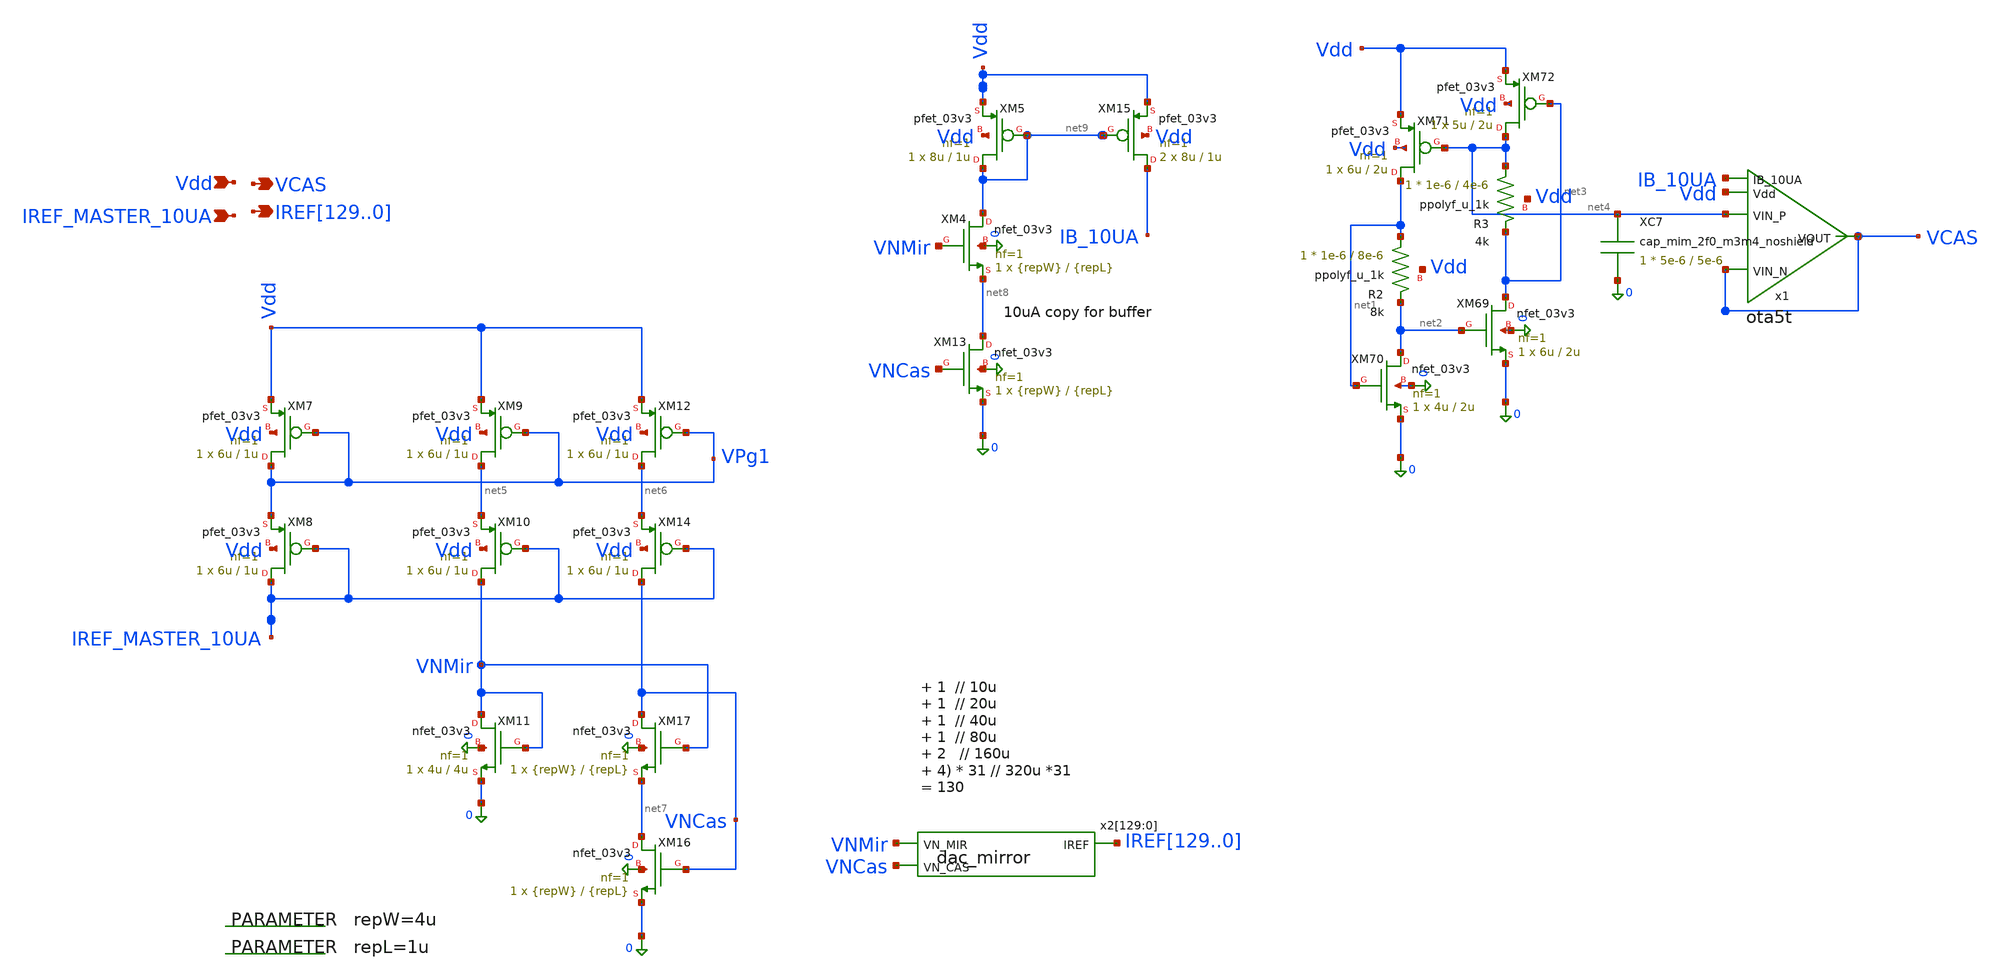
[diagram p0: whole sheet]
** sch_path: blocks/dac/iref/dac_iref.sch
**.subckt dac_iref Vdd VCAS
*+ IREF129,IREF128,IREF127,IREF126,IREF125,IREF124,IREF123,IREF122,IREF121,IREF120,IREF119,IREF118,IREF117,IREF116,IREF115,IREF114,IREF113,IREF112,IREF111,IREF110,IREF109,IREF108,IREF107,IREF106,IREF105,IREF104,IREF103,IREF102,IREF101,IREF100,IREF99,IREF98,IREF97,IREF96,IREF95,IREF94,IREF93,IREF92,IREF91,IREF90,IREF89,IREF88,IREF87,IREF86,IREF85,IREF84,IREF83,IREF82,IREF81,IREF80,IREF79,IREF78,IREF77,IREF76,IREF75,IREF74,IREF73,IREF72,IREF71,IREF70,IREF69,IREF68,IREF67,IREF66,IREF65,IREF64,IREF63,IREF62,IREF61,IREF60,IREF59,IREF58,IREF57,IREF56,IREF55,IREF54,IREF53,IREF52,IREF51,IREF50,IREF49,IREF48,IREF47,IREF46,IREF45,IREF44,IREF43,IREF42,IREF41,IREF40,IREF39,IREF38,IREF37,IREF36,IREF35,IREF34,IREF33,IREF32,IREF31,IREF30,IREF29,IREF28,IREF27,IREF26,IREF25,IREF24,IREF23,IREF22,IREF21,IREF20,IREF19,IREF18,IREF17,IREF16,IREF15,IREF14,IREF13,IREF12,IREF11,IREF10,IREF9,IREF8,IREF7,IREF6,IREF5,IREF4,IREF3,IREF2,IREF1,IREF0 IREF_MASTER_10UA
*.ipin Vdd
*.opin VCAS
*.opin
*+ IREF129,IREF128,IREF127,IREF126,IREF125,IREF124,IREF123,IREF122,IREF121,IREF120,IREF119,IREF118,IREF117,IREF116,IREF115,IREF114,IREF113,IREF112,IREF111,IREF110,IREF109,IREF108,IREF107,IREF106,IREF105,IREF104,IREF103,IREF102,IREF101,IREF100,IREF99,IREF98,IREF97,IREF96,IREF95,IREF94,IREF93,IREF92,IREF91,IREF90,IREF89,IREF88,IREF87,IREF86,IREF85,IREF84,IREF83,IREF82,IREF81,IREF80,IREF79,IREF78,IREF77,IREF76,IREF75,IREF74,IREF73,IREF72,IREF71,IREF70,IREF69,IREF68,IREF67,IREF66,IREF65,IREF64,IREF63,IREF62,IREF61,IREF60,IREF59,IREF58,IREF57,IREF56,IREF55,IREF54,IREF53,IREF52,IREF51,IREF50,IREF49,IREF48,IREF47,IREF46,IREF45,IREF44,IREF43,IREF42,IREF41,IREF40,IREF39,IREF38,IREF37,IREF36,IREF35,IREF34,IREF33,IREF32,IREF31,IREF30,IREF29,IREF28,IREF27,IREF26,IREF25,IREF24,IREF23,IREF22,IREF21,IREF20,IREF19,IREF18,IREF17,IREF16,IREF15,IREF14,IREF13,IREF12,IREF11,IREF10,IREF9,IREF8,IREF7,IREF6,IREF5,IREF4,IREF3,IREF2,IREF1,IREF0
*.ipin IREF_MASTER_10UA
XM69 net3 net2 0 0 nfet_03v3 L=2u W=6u nf=1 ad='int((nf+1)/2) * W/nf * 0.18u' as='int((nf+2)/2) * W/nf * 0.18u'
+ pd='2*int((nf+1)/2) * (W/nf + 0.18u)' ps='2*int((nf+2)/2) * (W/nf + 0.18u)' nrd='0.18u / W' nrs='0.18u / W'
+ sa=0 sb=0 sd=0 m=1
XM70 net2 net1 0 0 nfet_03v3 L=2u W=4u nf=1 ad='int((nf+1)/2) * W/nf * 0.18u' as='int((nf+2)/2) * W/nf * 0.18u'
+ pd='2*int((nf+1)/2) * (W/nf + 0.18u)' ps='2*int((nf+2)/2) * (W/nf + 0.18u)' nrd='0.18u / W' nrs='0.18u / W'
+ sa=0 sb=0 sd=0 m=1
XM71 net1 net4 Vdd Vdd pfet_03v3 L=2u W=6u nf=1 ad='int((nf+1)/2) * W/nf * 0.18u' as='int((nf+2)/2) * W/nf * 0.18u'
+ pd='2*int((nf+1)/2) * (W/nf + 0.18u)' ps='2*int((nf+2)/2) * (W/nf + 0.18u)' nrd='0.18u / W' nrs='0.18u / W'
+ sa=0 sb=0 sd=0 m=1
XM72 net4 net3 Vdd Vdd pfet_03v3 L=2u W=5u nf=1 ad='int((nf+1)/2) * W/nf * 0.18u' as='int((nf+2)/2) * W/nf * 0.18u'
+ pd='2*int((nf+1)/2) * (W/nf + 0.18u)' ps='2*int((nf+2)/2) * (W/nf + 0.18u)' nrd='0.18u / W' nrs='0.18u / W'
+ sa=0 sb=0 sd=0 m=1
x1 Vdd VCAS net4 VCAS IB_10UA ota5t
XC7 net4 0 cap_mim_2f0_m3m4_noshield c_width=5e-6 c_length=5e-6 m=1
XM7 VPg1 VPg1 Vdd Vdd pfet_03v3 L=1u W=6u nf=1 ad='int((nf+1)/2) * W/nf * 0.18u' as='int((nf+2)/2) * W/nf * 0.18u'
+ pd='2*int((nf+1)/2) * (W/nf + 0.18u)' ps='2*int((nf+2)/2) * (W/nf + 0.18u)' nrd='0.18u / W' nrs='0.18u / W'
+ sa=0 sb=0 sd=0 m=1
XM8 IREF_MASTER_10UA IREF_MASTER_10UA VPg1 Vdd pfet_03v3 L=1u W=6u nf=1 ad='int((nf+1)/2) * W/nf * 0.18u'
+ as='int((nf+2)/2) * W/nf * 0.18u' pd='2*int((nf+1)/2) * (W/nf + 0.18u)' ps='2*int((nf+2)/2) * (W/nf + 0.18u)'
+ nrd='0.18u / W' nrs='0.18u / W' sa=0 sb=0 sd=0 m=1
XM9 net5 VPg1 Vdd Vdd pfet_03v3 L=1u W=6u nf=1 ad='int((nf+1)/2) * W/nf * 0.18u' as='int((nf+2)/2) * W/nf * 0.18u'
+ pd='2*int((nf+1)/2) * (W/nf + 0.18u)' ps='2*int((nf+2)/2) * (W/nf + 0.18u)' nrd='0.18u / W' nrs='0.18u / W'
+ sa=0 sb=0 sd=0 m=1
XM10 VNMir IREF_MASTER_10UA net5 Vdd pfet_03v3 L=1u W=6u nf=1 ad='int((nf+1)/2) * W/nf * 0.18u' as='int((nf+2)/2) * W/nf * 0.18u'
+ pd='2*int((nf+1)/2) * (W/nf + 0.18u)' ps='2*int((nf+2)/2) * (W/nf + 0.18u)' nrd='0.18u / W' nrs='0.18u / W'
+ sa=0 sb=0 sd=0 m=1
XM11 VNMir VNMir 0 0 nfet_03v3 L=4u W=4u nf=1 ad='int((nf+1)/2) * W/nf * 0.18u' as='int((nf+2)/2) * W/nf * 0.18u'
+ pd='2*int((nf+1)/2) * (W/nf + 0.18u)' ps='2*int((nf+2)/2) * (W/nf + 0.18u)' nrd='0.18u / W' nrs='0.18u / W'
+ sa=0 sb=0 sd=0 m=1
XM12 net6 VPg1 Vdd Vdd pfet_03v3 L=1u W=6u nf=1 ad='int((nf+1)/2) * W/nf * 0.18u' as='int((nf+2)/2) * W/nf * 0.18u'
+ pd='2*int((nf+1)/2) * (W/nf + 0.18u)' ps='2*int((nf+2)/2) * (W/nf + 0.18u)' nrd='0.18u / W' nrs='0.18u / W'
+ sa=0 sb=0 sd=0 m=1
XM14 VNCas IREF_MASTER_10UA net6 Vdd pfet_03v3 L=1u W=6u nf=1 ad='int((nf+1)/2) * W/nf * 0.18u' as='int((nf+2)/2) * W/nf * 0.18u'
+ pd='2*int((nf+1)/2) * (W/nf + 0.18u)' ps='2*int((nf+2)/2) * (W/nf + 0.18u)' nrd='0.18u / W' nrs='0.18u / W'
+ sa=0 sb=0 sd=0 m=1
XM16 net7 VNCas 0 0 nfet_03v3 L={repL} W={repW} nf=1 ad='int((nf+1)/2) * W/nf * 0.18u' as='int((nf+2)/2) * W/nf * 0.18u'
+ pd='2*int((nf+1)/2) * (W/nf + 0.18u)' ps='2*int((nf+2)/2) * (W/nf + 0.18u)' nrd='0.18u / W' nrs='0.18u / W'
+ sa=0 sb=0 sd=0 m=1
XM17 VNCas VNMir net7 0 nfet_03v3 L={repL} W={repW} nf=1 ad='int((nf+1)/2) * W/nf * 0.18u' as='int((nf+2)/2) * W/nf * 0.18u'
+ pd='2*int((nf+1)/2) * (W/nf + 0.18u)' ps='2*int((nf+2)/2) * (W/nf + 0.18u)' nrd='0.18u / W' nrs='0.18u / W'
+ sa=0 sb=0 sd=0 m=1
XM4 net9 VNMir net8 0 nfet_03v3 L={repL} W={repW} nf=1 ad='int((nf+1)/2) * W/nf * 0.18u' as='int((nf+2)/2) * W/nf * 0.18u'
+ pd='2*int((nf+1)/2) * (W/nf + 0.18u)' ps='2*int((nf+2)/2) * (W/nf + 0.18u)' nrd='0.18u / W' nrs='0.18u / W'
+ sa=0 sb=0 sd=0 m=1
XM5 net9 net9 Vdd Vdd pfet_03v3 L=1u W=8u nf=1 ad='int((nf+1)/2) * W/nf * 0.18u' as='int((nf+2)/2) * W/nf * 0.18u'
+ pd='2*int((nf+1)/2) * (W/nf + 0.18u)' ps='2*int((nf+2)/2) * (W/nf + 0.18u)' nrd='0.18u / W' nrs='0.18u / W'
+ sa=0 sb=0 sd=0 m=1
XM13 net8 VNCas 0 0 nfet_03v3 L={repL} W={repW} nf=1 ad='int((nf+1)/2) * W/nf * 0.18u' as='int((nf+2)/2) * W/nf * 0.18u'
+ pd='2*int((nf+1)/2) * (W/nf + 0.18u)' ps='2*int((nf+2)/2) * (W/nf + 0.18u)' nrd='0.18u / W' nrs='0.18u / W'
+ sa=0 sb=0 sd=0 m=1
XR3 net4 net3 Vdd ppolyf_u_1k r_width=1e-6 r_length=4e-6 m=1
XR2 net1 net2 Vdd ppolyf_u_1k r_width=1e-6 r_length=8e-6 m=1
.param repW=4u
.param repL=1u
XM15 IB_10UA net9 Vdd Vdd pfet_03v3 L=1u W=8u nf=1 ad='int((nf+1)/2) * W/nf * 0.18u' as='int((nf+2)/2) * W/nf * 0.18u'
+ pd='2*int((nf+1)/2) * (W/nf + 0.18u)' ps='2*int((nf+2)/2) * (W/nf + 0.18u)' nrd='0.18u / W' nrs='0.18u / W'
+ sa=0 sb=0 sd=0 m=2
x2[129] VNMir IREF129 VNCas dac_mirror
x2[128] VNMir IREF128 VNCas dac_mirror
x2[127] VNMir IREF127 VNCas dac_mirror
x2[126] VNMir IREF126 VNCas dac_mirror
x2[125] VNMir IREF125 VNCas dac_mirror
x2[124] VNMir IREF124 VNCas dac_mirror
x2[123] VNMir IREF123 VNCas dac_mirror
x2[122] VNMir IREF122 VNCas dac_mirror
x2[121] VNMir IREF121 VNCas dac_mirror
x2[120] VNMir IREF120 VNCas dac_mirror
x2[119] VNMir IREF119 VNCas dac_mirror
x2[118] VNMir IREF118 VNCas dac_mirror
x2[117] VNMir IREF117 VNCas dac_mirror
x2[116] VNMir IREF116 VNCas dac_mirror
x2[115] VNMir IREF115 VNCas dac_mirror
x2[114] VNMir IREF114 VNCas dac_mirror
x2[113] VNMir IREF113 VNCas dac_mirror
x2[112] VNMir IREF112 VNCas dac_mirror
x2[111] VNMir IREF111 VNCas dac_mirror
x2[110] VNMir IREF110 VNCas dac_mirror
x2[109] VNMir IREF109 VNCas dac_mirror
x2[108] VNMir IREF108 VNCas dac_mirror
x2[107] VNMir IREF107 VNCas dac_mirror
x2[106] VNMir IREF106 VNCas dac_mirror
x2[105] VNMir IREF105 VNCas dac_mirror
x2[104] VNMir IREF104 VNCas dac_mirror
x2[103] VNMir IREF103 VNCas dac_mirror
x2[102] VNMir IREF102 VNCas dac_mirror
x2[101] VNMir IREF101 VNCas dac_mirror
x2[100] VNMir IREF100 VNCas dac_mirror
x2[99] VNMir IREF99 VNCas dac_mirror
x2[98] VNMir IREF98 VNCas dac_mirror
x2[97] VNMir IREF97 VNCas dac_mirror
x2[96] VNMir IREF96 VNCas dac_mirror
x2[95] VNMir IREF95 VNCas dac_mirror
x2[94] VNMir IREF94 VNCas dac_mirror
x2[93] VNMir IREF93 VNCas dac_mirror
x2[92] VNMir IREF92 VNCas dac_mirror
x2[91] VNMir IREF91 VNCas dac_mirror
x2[90] VNMir IREF90 VNCas dac_mirror
x2[89] VNMir IREF89 VNCas dac_mirror
x2[88] VNMir IREF88 VNCas dac_mirror
x2[87] VNMir IREF87 VNCas dac_mirror
x2[86] VNMir IREF86 VNCas dac_mirror
x2[85] VNMir IREF85 VNCas dac_mirror
x2[84] VNMir IREF84 VNCas dac_mirror
x2[83] VNMir IREF83 VNCas dac_mirror
x2[82] VNMir IREF82 VNCas dac_mirror
x2[81] VNMir IREF81 VNCas dac_mirror
x2[80] VNMir IREF80 VNCas dac_mirror
x2[79] VNMir IREF79 VNCas dac_mirror
x2[78] VNMir IREF78 VNCas dac_mirror
x2[77] VNMir IREF77 VNCas dac_mirror
x2[76] VNMir IREF76 VNCas dac_mirror
x2[75] VNMir IREF75 VNCas dac_mirror
x2[74] VNMir IREF74 VNCas dac_mirror
x2[73] VNMir IREF73 VNCas dac_mirror
x2[72] VNMir IREF72 VNCas dac_mirror
x2[71] VNMir IREF71 VNCas dac_mirror
x2[70] VNMir IREF70 VNCas dac_mirror
x2[69] VNMir IREF69 VNCas dac_mirror
x2[68] VNMir IREF68 VNCas dac_mirror
x2[67] VNMir IREF67 VNCas dac_mirror
x2[66] VNMir IREF66 VNCas dac_mirror
x2[65] VNMir IREF65 VNCas dac_mirror
x2[64] VNMir IREF64 VNCas dac_mirror
x2[63] VNMir IREF63 VNCas dac_mirror
x2[62] VNMir IREF62 VNCas dac_mirror
x2[61] VNMir IREF61 VNCas dac_mirror
x2[60] VNMir IREF60 VNCas dac_mirror
x2[59] VNMir IREF59 VNCas dac_mirror
x2[58] VNMir IREF58 VNCas dac_mirror
x2[57] VNMir IREF57 VNCas dac_mirror
x2[56] VNMir IREF56 VNCas dac_mirror
x2[55] VNMir IREF55 VNCas dac_mirror
x2[54] VNMir IREF54 VNCas dac_mirror
x2[53] VNMir IREF53 VNCas dac_mirror
x2[52] VNMir IREF52 VNCas dac_mirror
x2[51] VNMir IREF51 VNCas dac_mirror
x2[50] VNMir IREF50 VNCas dac_mirror
x2[49] VNMir IREF49 VNCas dac_mirror
x2[48] VNMir IREF48 VNCas dac_mirror
x2[47] VNMir IREF47 VNCas dac_mirror
x2[46] VNMir IREF46 VNCas dac_mirror
x2[45] VNMir IREF45 VNCas dac_mirror
x2[44] VNMir IREF44 VNCas dac_mirror
x2[43] VNMir IREF43 VNCas dac_mirror
x2[42] VNMir IREF42 VNCas dac_mirror
x2[41] VNMir IREF41 VNCas dac_mirror
x2[40] VNMir IREF40 VNCas dac_mirror
x2[39] VNMir IREF39 VNCas dac_mirror
x2[38] VNMir IREF38 VNCas dac_mirror
x2[37] VNMir IREF37 VNCas dac_mirror
x2[36] VNMir IREF36 VNCas dac_mirror
x2[35] VNMir IREF35 VNCas dac_mirror
x2[34] VNMir IREF34 VNCas dac_mirror
x2[33] VNMir IREF33 VNCas dac_mirror
x2[32] VNMir IREF32 VNCas dac_mirror
x2[31] VNMir IREF31 VNCas dac_mirror
x2[30] VNMir IREF30 VNCas dac_mirror
x2[29] VNMir IREF29 VNCas dac_mirror
x2[28] VNMir IREF28 VNCas dac_mirror
x2[27] VNMir IREF27 VNCas dac_mirror
x2[26] VNMir IREF26 VNCas dac_mirror
x2[25] VNMir IREF25 VNCas dac_mirror
x2[24] VNMir IREF24 VNCas dac_mirror
x2[23] VNMir IREF23 VNCas dac_mirror
x2[22] VNMir IREF22 VNCas dac_mirror
x2[21] VNMir IREF21 VNCas dac_mirror
x2[20] VNMir IREF20 VNCas dac_mirror
x2[19] VNMir IREF19 VNCas dac_mirror
x2[18] VNMir IREF18 VNCas dac_mirror
x2[17] VNMir IREF17 VNCas dac_mirror
x2[16] VNMir IREF16 VNCas dac_mirror
x2[15] VNMir IREF15 VNCas dac_mirror
x2[14] VNMir IREF14 VNCas dac_mirror
x2[13] VNMir IREF13 VNCas dac_mirror
x2[12] VNMir IREF12 VNCas dac_mirror
x2[11] VNMir IREF11 VNCas dac_mirror
x2[10] VNMir IREF10 VNCas dac_mirror
x2[9] VNMir IREF9 VNCas dac_mirror
x2[8] VNMir IREF8 VNCas dac_mirror
x2[7] VNMir IREF7 VNCas dac_mirror
x2[6] VNMir IREF6 VNCas dac_mirror
x2[5] VNMir IREF5 VNCas dac_mirror
x2[4] VNMir IREF4 VNCas dac_mirror
x2[3] VNMir IREF3 VNCas dac_mirror
x2[2] VNMir IREF2 VNCas dac_mirror
x2[1] VNMir IREF1 VNCas dac_mirror
x2[0] VNMir IREF0 VNCas dac_mirror
**.ends

* expanding   symbol:  common/ota5t.sym # of pins=5
** sym_path: blocks/dac/common/ota5t.sym
** sch_path: blocks/dac/common/ota5t.sch
.subckt ota5t Vdd VIN_N VIN_P VOUT IB_10UA
*.ipin VIN_P
*.ipin VIN_N
*.opin VOUT
*.ipin Vdd
*.ipin IB_10UA
XM16 VOUT net1 0 0 nfet_03v3 L=1u W=2u nf=1 ad='int((nf+1)/2) * W/nf * 0.18u' as='int((nf+2)/2) * W/nf * 0.18u'
+ pd='2*int((nf+1)/2) * (W/nf + 0.18u)' ps='2*int((nf+2)/2) * (W/nf + 0.18u)' nrd='0.18u / W' nrs='0.18u / W'
+ sa=0 sb=0 sd=0 m=1
XM1 VOUT VIN_N IB_10UA Vdd pfet_03v3 L=1u W=4u nf=1 ad='int((nf+1)/2) * W/nf * 0.18u' as='int((nf+2)/2) * W/nf * 0.18u'
+ pd='2*int((nf+1)/2) * (W/nf + 0.18u)' ps='2*int((nf+2)/2) * (W/nf + 0.18u)' nrd='0.18u / W' nrs='0.18u / W'
+ sa=0 sb=0 sd=0 m=1
XM19 net1 VIN_P IB_10UA Vdd pfet_03v3 L=1u W=4u nf=1 ad='int((nf+1)/2) * W/nf * 0.18u' as='int((nf+2)/2) * W/nf * 0.18u'
+ pd='2*int((nf+1)/2) * (W/nf + 0.18u)' ps='2*int((nf+2)/2) * (W/nf + 0.18u)' nrd='0.18u / W' nrs='0.18u / W'
+ sa=0 sb=0 sd=0 m=1
XM22 net1 net1 0 0 nfet_03v3 L=1u W=2u nf=1 ad='int((nf+1)/2) * W/nf * 0.18u' as='int((nf+2)/2) * W/nf * 0.18u'
+ pd='2*int((nf+1)/2) * (W/nf + 0.18u)' ps='2*int((nf+2)/2) * (W/nf + 0.18u)' nrd='0.18u / W' nrs='0.18u / W'
+ sa=0 sb=0 sd=0 m=1
.ends


* expanding   symbol:  iref/dac_mirror.sym # of pins=3
** sym_path: blocks/dac/iref/dac_mirror.sym
** sch_path: blocks/dac/iref/dac_mirror.sch
.subckt dac_mirror VN_MIR IREF VN_CAS
*.ipin VN_MIR
*.opin IREF
*.ipin VN_CAS
XM1 IREF VN_MIR net1 0 nfet_03v3 L={repL} W={repW} nf=1 ad='int((nf+1)/2) * W/nf * 0.18u' as='int((nf+2)/2) * W/nf * 0.18u'
+ pd='2*int((nf+1)/2) * (W/nf + 0.18u)' ps='2*int((nf+2)/2) * (W/nf + 0.18u)' nrd='0.18u / W' nrs='0.18u / W'
+ sa=0 sb=0 sd=0 m=1
XM2 net1 VN_CAS 0 0 nfet_03v3 L={repL} W={repW} nf=1 ad='int((nf+1)/2) * W/nf * 0.18u' as='int((nf+2)/2) * W/nf * 0.18u'
+ pd='2*int((nf+1)/2) * (W/nf + 0.18u)' ps='2*int((nf+2)/2) * (W/nf + 0.18u)' nrd='0.18u / W' nrs='0.18u / W'
+ sa=0 sb=0 sd=0 m=1
.ends

.end
